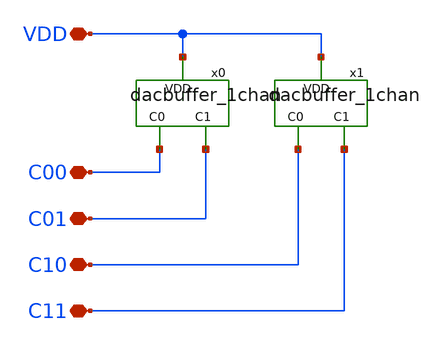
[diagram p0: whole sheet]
** sch_path: xschem/dacendbuffer.sch
**.subckt dacendbuffer VDD C00 C01 C10 C11
*.iopin VDD
*.iopin C00
*.iopin C01
*.iopin C10
*.iopin C11
x0 VDD C00 C01 dacbuffer_1chan
x1 VDD C10 C11 dacbuffer_1chan
**.ends

* expanding   symbol:  dacbuffer_1chan.sym # of pins=3
** sym_path: xschem/dacbuffer_1chan.sym
** sch_path: xschem/dacbuffer_1chan.sch
.subckt dacbuffer_1chan VDD C0 C1
*.iopin VDD
*.iopin C0
*.iopin C1
XM1 VDD g1 VDD VDD sg13_hv_pmos w=14.6u l=4.04u ng=1 m=1 mm_ok=1
XM0 VDD g0 VDD VDD sg13_hv_pmos w=14.6u l=4.04u ng=1 m=1 mm_ok=1
V0 g0 C0 0
.save i(v0)
V1 g1 C1 0
.save i(v1)
.ends

.end
